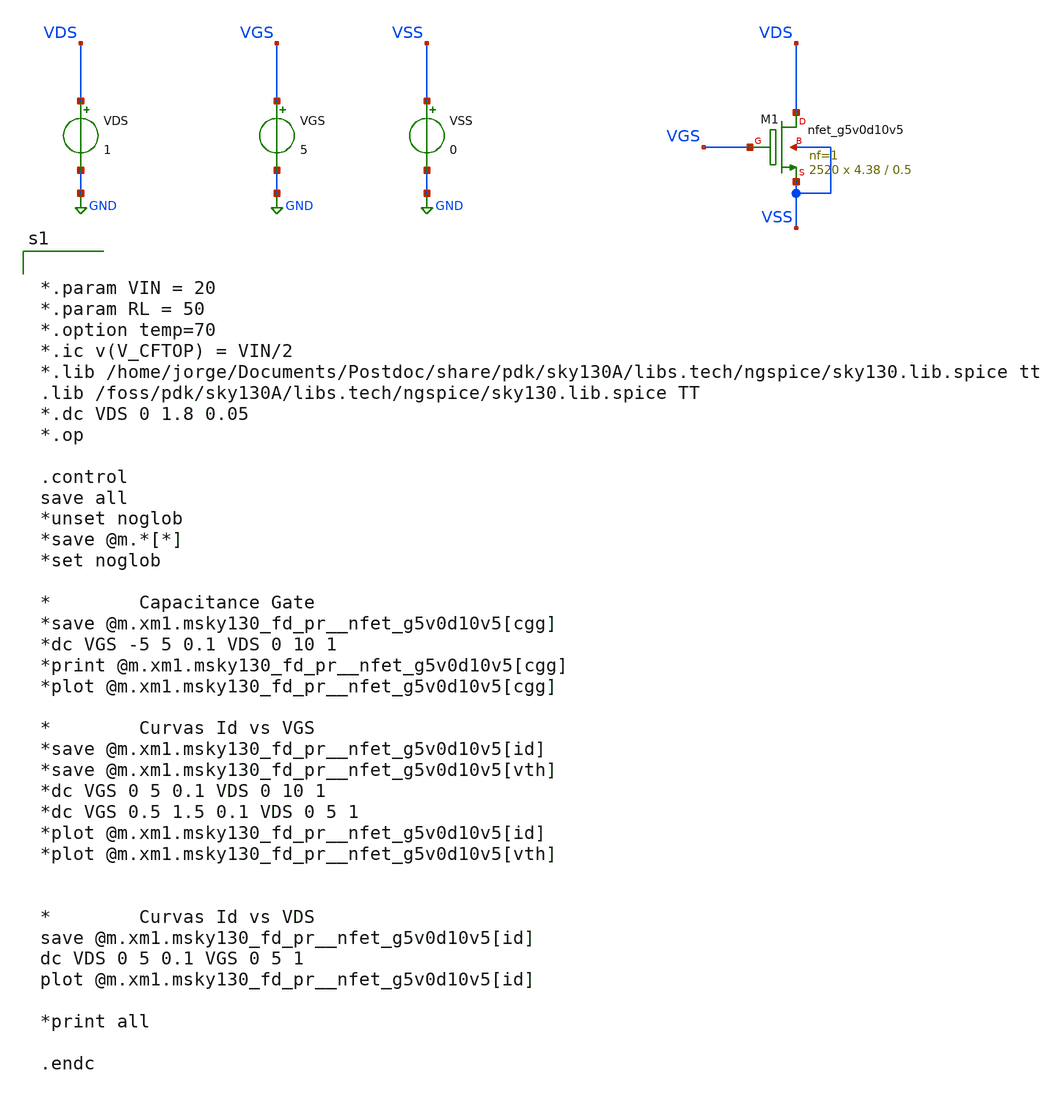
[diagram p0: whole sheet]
** sch_path: xschem/dev_switches/NMOSSW_full_OPsweep_v1p2_20220828.sch
**.subckt NMOSSW_full_OPsweep_v1p2_20220828
VGS VGS GND 5
VSS VSS GND 0
VDS VDS GND 1
XM1 VDS VGS VSS VSS sky130_fd_pr__nfet_g5v0d10v5 L=0.5 W=4.38 nf=1 ad='int((nf+1)/2) * W/nf * 0.29' as='int((nf+2)/2) * W/nf * 0.29'
+ pd='2*int((nf+1)/2) * (W/nf + 0.29)' ps='2*int((nf+2)/2) * (W/nf + 0.29)' nrd='0.29 / W' nrs='0.29 / W'
+ sa=0 sb=0 sd=0 mult=2520 m=2520
**** begin user architecture code


*.param VIN = 20
*.param RL = 50
*.option temp=70
*.ic v(V_CFTOP) = VIN/2
*.lib /home/jorge/Documents/Postdoc/share/pdk/sky130A/libs.tech/ngspice/sky130.lib.spice tt
.lib /foss/pdk/sky130A/libs.tech/ngspice/sky130.lib.spice TT
*.dc VDS 0 1.8 0.05
*.op

.control
save all
*unset noglob
*save @m.*[*]
*set noglob

*		Capacitance Gate
*save @m.xm1.msky130_fd_pr__nfet_g5v0d10v5[cgg]
*dc VGS -5 5 0.1 VDS 0 10 1
*print @m.xm1.msky130_fd_pr__nfet_g5v0d10v5[cgg]
*plot @m.xm1.msky130_fd_pr__nfet_g5v0d10v5[cgg]

*		Curvas Id vs VGS
*save @m.xm1.msky130_fd_pr__nfet_g5v0d10v5[id]
*save @m.xm1.msky130_fd_pr__nfet_g5v0d10v5[vth]
*dc VGS 0 5 0.1 VDS 0 10 1
*dc VGS 0.5 1.5 0.1 VDS 0 5 1
*plot @m.xm1.msky130_fd_pr__nfet_g5v0d10v5[id]
*plot @m.xm1.msky130_fd_pr__nfet_g5v0d10v5[vth]


*		Curvas Id vs VDS
save @m.xm1.msky130_fd_pr__nfet_g5v0d10v5[id]
dc VDS 0 5 0.1 VGS 0 5 1
plot @m.xm1.msky130_fd_pr__nfet_g5v0d10v5[id]

*print all

.endc



**** end user architecture code
**.ends
.GLOBAL GND
.end
